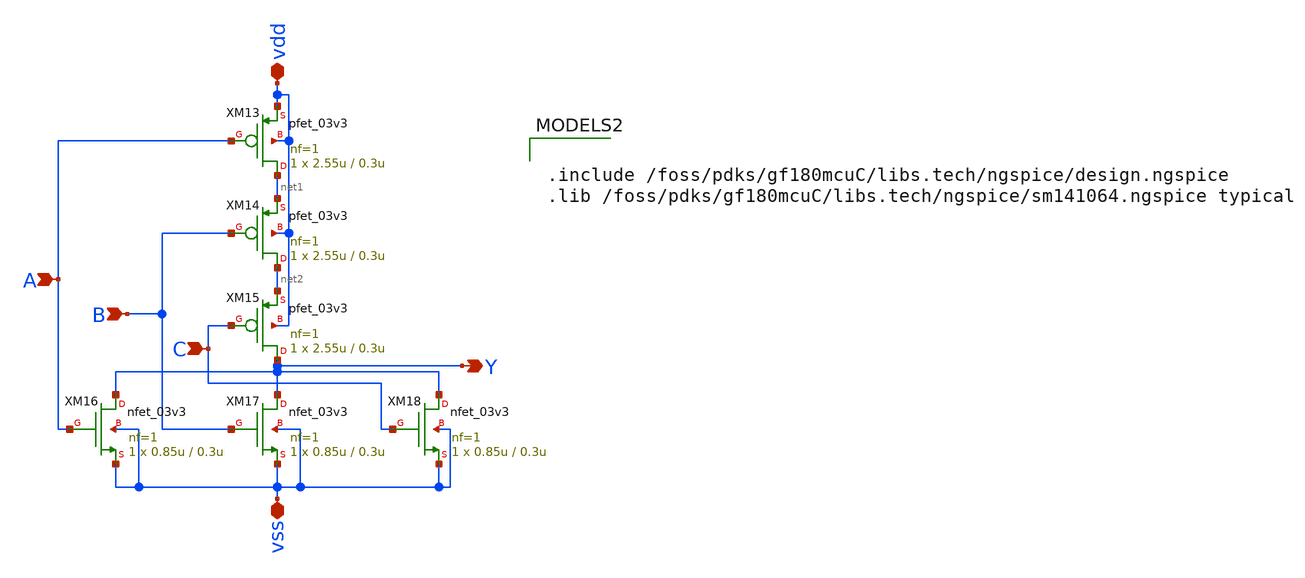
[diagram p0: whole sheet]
** sch_path: Cells/NOR3_1/nor_3.sch
**.subckt nor_3 vdd vss B A C Y
*.iopin vdd
*.iopin vss
*.ipin B
*.ipin A
*.ipin C
*.opin Y
XM13 net1 A vdd vdd pfet_03v3 L=0.3u W=2.55u nf=1 ad='int((nf+1)/2) * W/nf * 0.18u' as='int((nf+2)/2) * W/nf * 0.18u'
+ pd='2*int((nf+1)/2) * (W/nf + 0.18u)' ps='2*int((nf+2)/2) * (W/nf + 0.18u)' nrd='0.18u / W' nrs='0.18u / W'
+ sa=0 sb=0 sd=0 m=1
XM14 net2 B net1 vdd pfet_03v3 L=0.3u W=2.55u nf=1 ad='int((nf+1)/2) * W/nf * 0.18u' as='int((nf+2)/2) * W/nf * 0.18u'
+ pd='2*int((nf+1)/2) * (W/nf + 0.18u)' ps='2*int((nf+2)/2) * (W/nf + 0.18u)' nrd='0.18u / W' nrs='0.18u / W'
+ sa=0 sb=0 sd=0 m=1
XM15 Y C net2 vdd pfet_03v3 L=0.3u W=2.55u nf=1 ad='int((nf+1)/2) * W/nf * 0.18u' as='int((nf+2)/2) * W/nf * 0.18u'
+ pd='2*int((nf+1)/2) * (W/nf + 0.18u)' ps='2*int((nf+2)/2) * (W/nf + 0.18u)' nrd='0.18u / W' nrs='0.18u / W'
+ sa=0 sb=0 sd=0 m=1
XM16 Y A vss vss nfet_03v3 L=0.3u W=0.85u nf=1 ad='int((nf+1)/2) * W/nf * 0.18u' as='int((nf+2)/2) * W/nf * 0.18u'
+ pd='2*int((nf+1)/2) * (W/nf + 0.18u)' ps='2*int((nf+2)/2) * (W/nf + 0.18u)' nrd='0.18u / W' nrs='0.18u / W'
+ sa=0 sb=0 sd=0 m=1
XM17 Y B vss vss nfet_03v3 L=0.3u W=0.85u nf=1 ad='int((nf+1)/2) * W/nf * 0.18u' as='int((nf+2)/2) * W/nf * 0.18u'
+ pd='2*int((nf+1)/2) * (W/nf + 0.18u)' ps='2*int((nf+2)/2) * (W/nf + 0.18u)' nrd='0.18u / W' nrs='0.18u / W'
+ sa=0 sb=0 sd=0 m=1
XM18 Y C vss vss nfet_03v3 L=0.3u W=0.85u nf=1 ad='int((nf+1)/2) * W/nf * 0.18u' as='int((nf+2)/2) * W/nf * 0.18u'
+ pd='2*int((nf+1)/2) * (W/nf + 0.18u)' ps='2*int((nf+2)/2) * (W/nf + 0.18u)' nrd='0.18u / W' nrs='0.18u / W'
+ sa=0 sb=0 sd=0 m=1
**** begin user architecture code

.include /foss/pdks/gf180mcuC/libs.tech/ngspice/design.ngspice
.lib /foss/pdks/gf180mcuC/libs.tech/ngspice/sm141064.ngspice typical

**** end user architecture code
**.ends
.end
